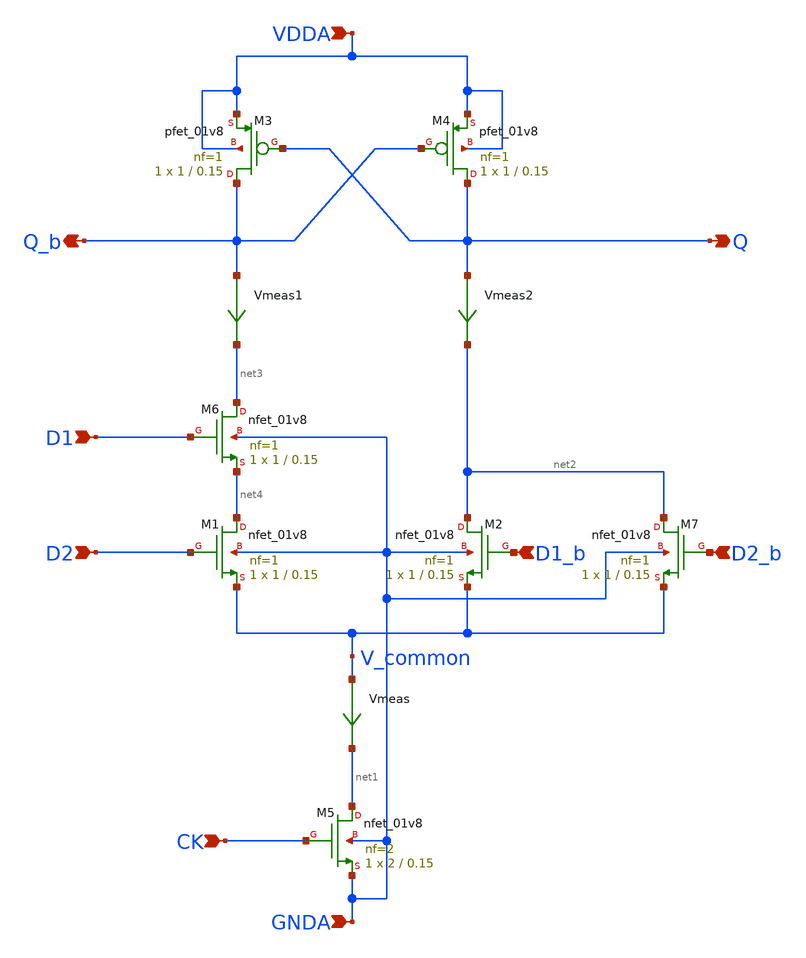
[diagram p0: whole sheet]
** sch_path: projects/pll/divider/xschem_ngspice/xcp_latch_nand.sch
**.subckt xcp_latch_nand D2 Q D1_b CK Q_b VDDA GNDA D1 D2_b
*.ipin D2
*.opin Q
*.ipin D1_b
*.ipin CK
*.opin Q_b
*.ipin VDDA
*.ipin GNDA
*.ipin D1
*.ipin D2_b
XM5 net1 CK GNDA GNDA sky130_fd_pr__nfet_01v8 L=0.15 W=2 nf=2 ad='int((nf+1)/2) * W/nf * 0.29' as='int((nf+2)/2) * W/nf * 0.29'
+ pd='2*int((nf+1)/2) * (W/nf + 0.29)' ps='2*int((nf+2)/2) * (W/nf + 0.29)' nrd='0.29 / W' nrs='0.29 / W'
+ sa=0 sb=0 sd=0 mult=1 m=1
XM1 net4 D2 V_common GNDA sky130_fd_pr__nfet_01v8 L=0.15 W=1 nf=1 ad='int((nf+1)/2) * W/nf * 0.29' as='int((nf+2)/2) * W/nf * 0.29'
+ pd='2*int((nf+1)/2) * (W/nf + 0.29)' ps='2*int((nf+2)/2) * (W/nf + 0.29)' nrd='0.29 / W' nrs='0.29 / W'
+ sa=0 sb=0 sd=0 mult=1 m=1
XM2 net2 D1_b V_common GNDA sky130_fd_pr__nfet_01v8 L=0.15 W=1 nf=1 ad='int((nf+1)/2) * W/nf * 0.29'
+ as='int((nf+2)/2) * W/nf * 0.29' pd='2*int((nf+1)/2) * (W/nf + 0.29)' ps='2*int((nf+2)/2) * (W/nf + 0.29)'
+ nrd='0.29 / W' nrs='0.29 / W' sa=0 sb=0 sd=0 mult=1 m=1
Vmeas V_common net1 0
.save i(vmeas)
Vmeas1 Q_b net3 0
.save i(vmeas1)
Vmeas2 Q net2 0
.save i(vmeas2)
XM3 Q_b Q VDDA VDDA sky130_fd_pr__pfet_01v8 L=0.15 W=1 nf=1 ad='int((nf+1)/2) * W/nf * 0.29' as='int((nf+2)/2) * W/nf * 0.29'
+ pd='2*int((nf+1)/2) * (W/nf + 0.29)' ps='2*int((nf+2)/2) * (W/nf + 0.29)' nrd='0.29 / W' nrs='0.29 / W'
+ sa=0 sb=0 sd=0 mult=1 m=1
XM4 Q Q_b VDDA VDDA sky130_fd_pr__pfet_01v8 L=0.15 W=1 nf=1 ad='int((nf+1)/2) * W/nf * 0.29' as='int((nf+2)/2) * W/nf * 0.29'
+ pd='2*int((nf+1)/2) * (W/nf + 0.29)' ps='2*int((nf+2)/2) * (W/nf + 0.29)' nrd='0.29 / W' nrs='0.29 / W'
+ sa=0 sb=0 sd=0 mult=1 m=1
XM6 net3 D1 net4 GNDA sky130_fd_pr__nfet_01v8 L=0.15 W=1 nf=1 ad='int((nf+1)/2) * W/nf * 0.29' as='int((nf+2)/2) * W/nf * 0.29'
+ pd='2*int((nf+1)/2) * (W/nf + 0.29)' ps='2*int((nf+2)/2) * (W/nf + 0.29)' nrd='0.29 / W' nrs='0.29 / W'
+ sa=0 sb=0 sd=0 mult=1 m=1
XM7 net2 D2_b V_common GNDA sky130_fd_pr__nfet_01v8 L=0.15 W=1 nf=1 ad='int((nf+1)/2) * W/nf * 0.29'
+ as='int((nf+2)/2) * W/nf * 0.29' pd='2*int((nf+1)/2) * (W/nf + 0.29)' ps='2*int((nf+2)/2) * (W/nf + 0.29)'
+ nrd='0.29 / W' nrs='0.29 / W' sa=0 sb=0 sd=0 mult=1 m=1
**.ends
.end
